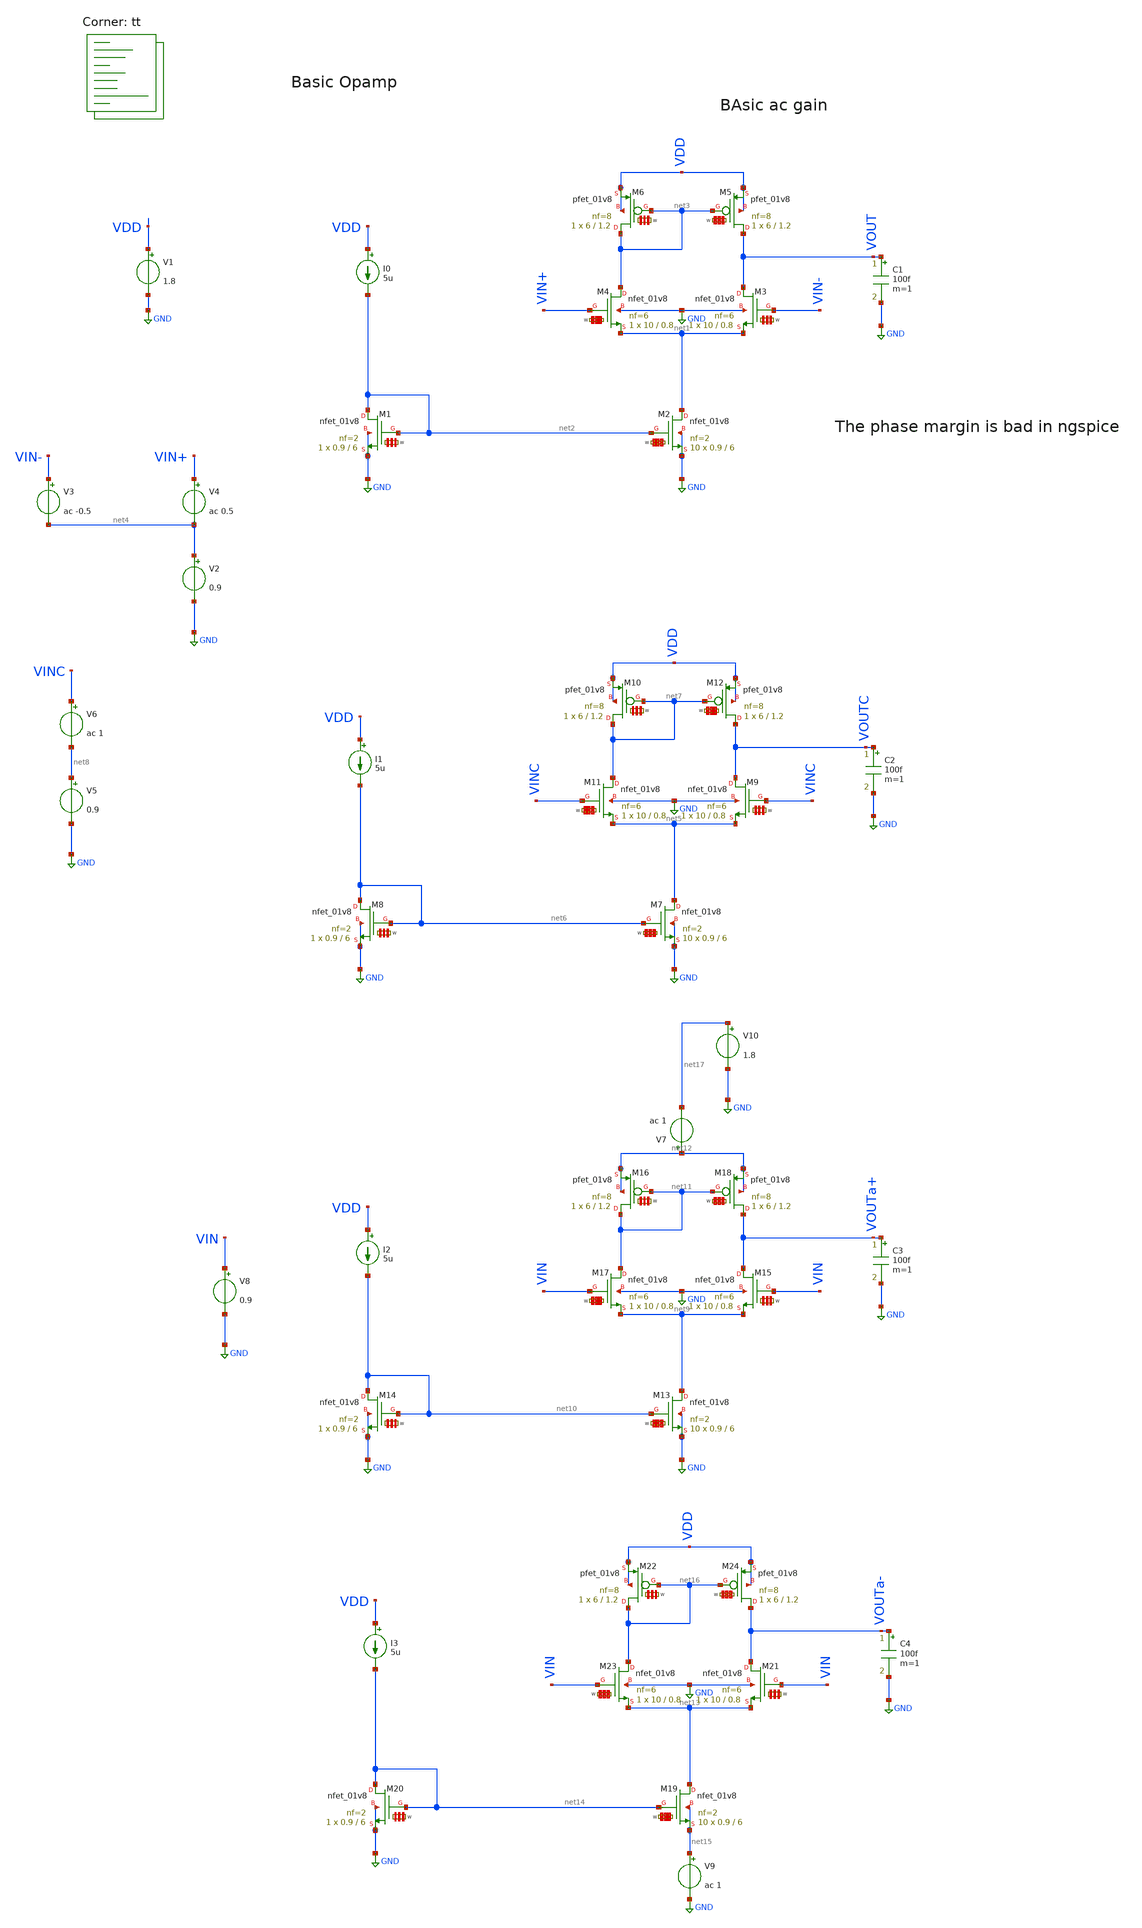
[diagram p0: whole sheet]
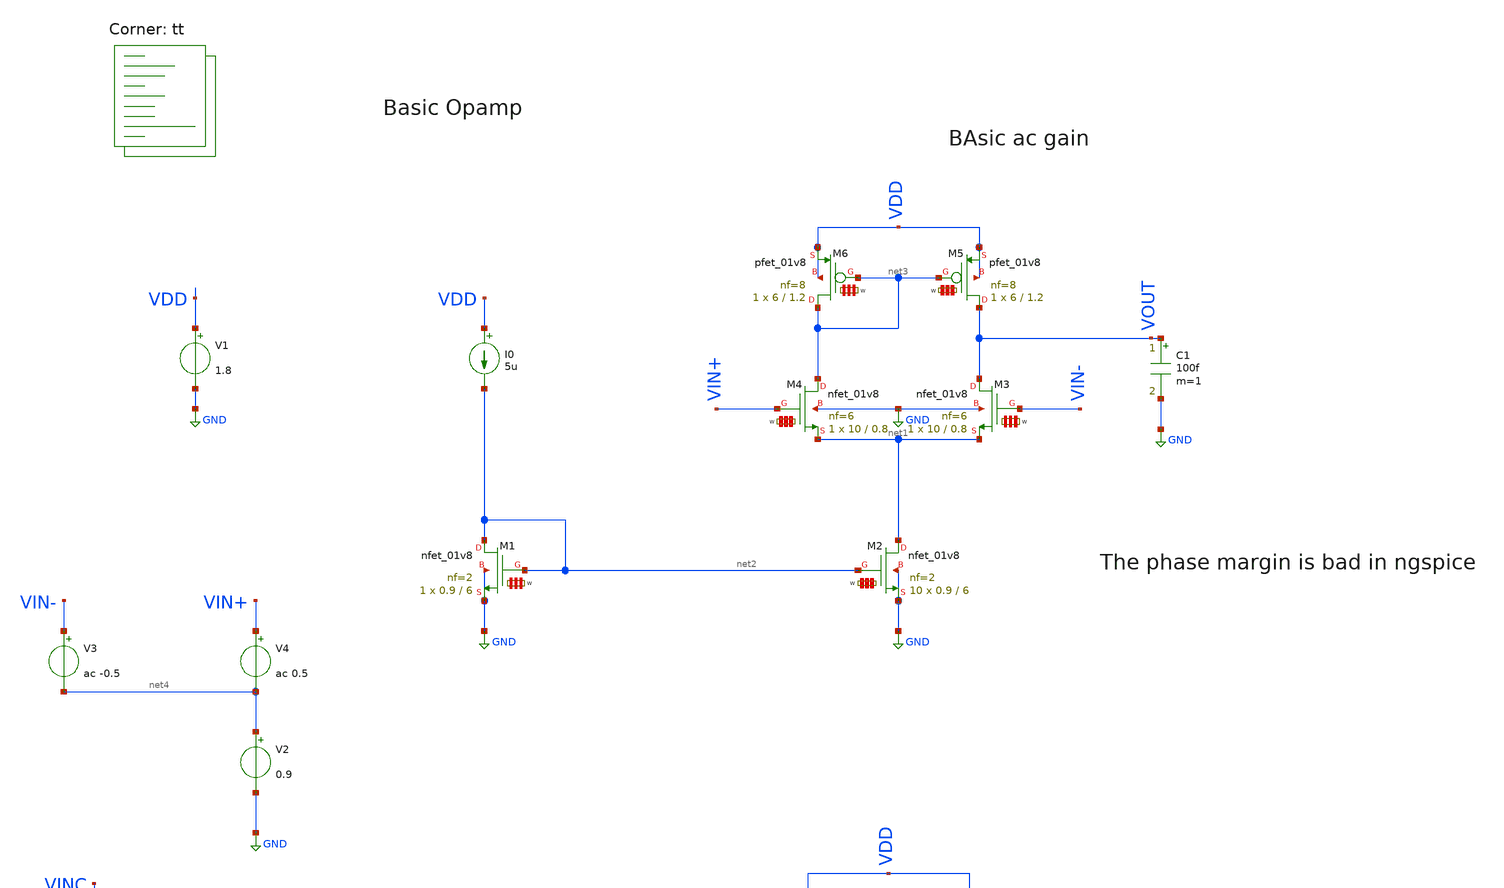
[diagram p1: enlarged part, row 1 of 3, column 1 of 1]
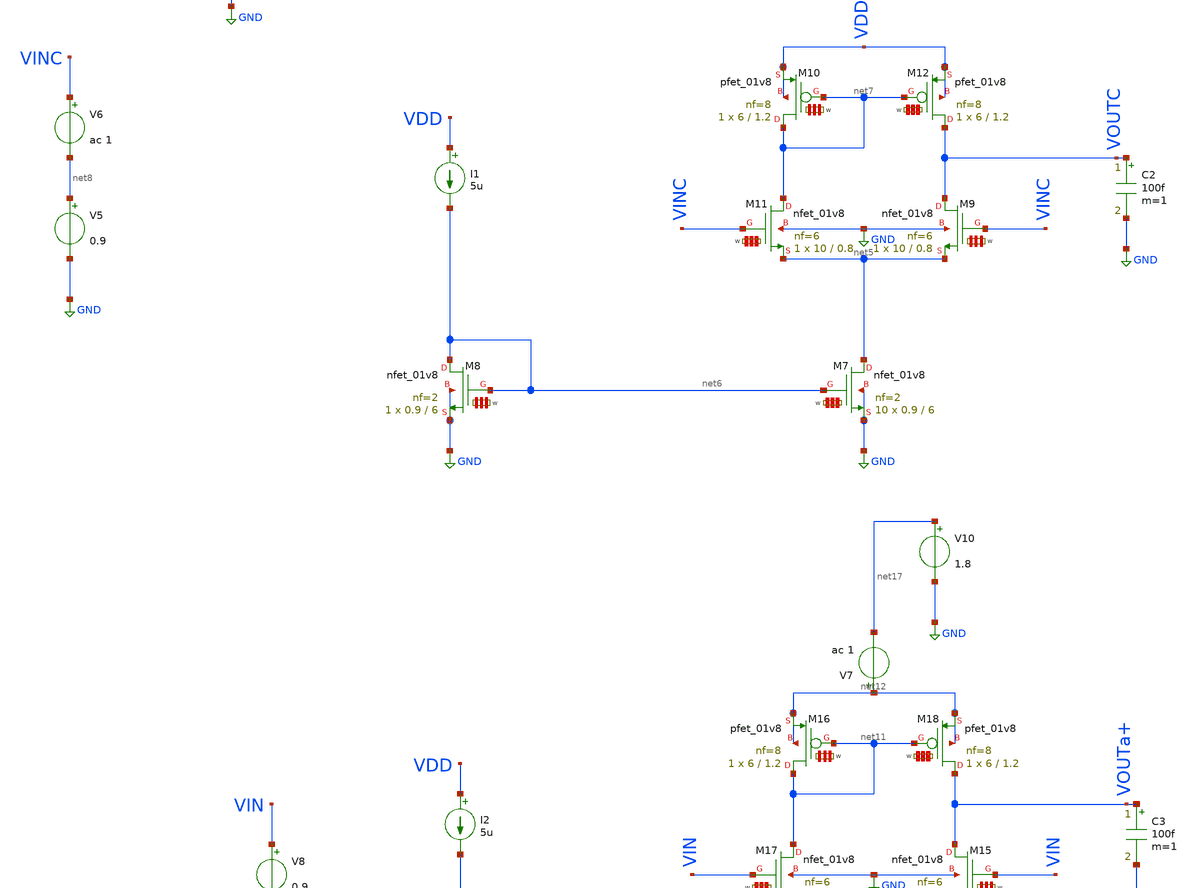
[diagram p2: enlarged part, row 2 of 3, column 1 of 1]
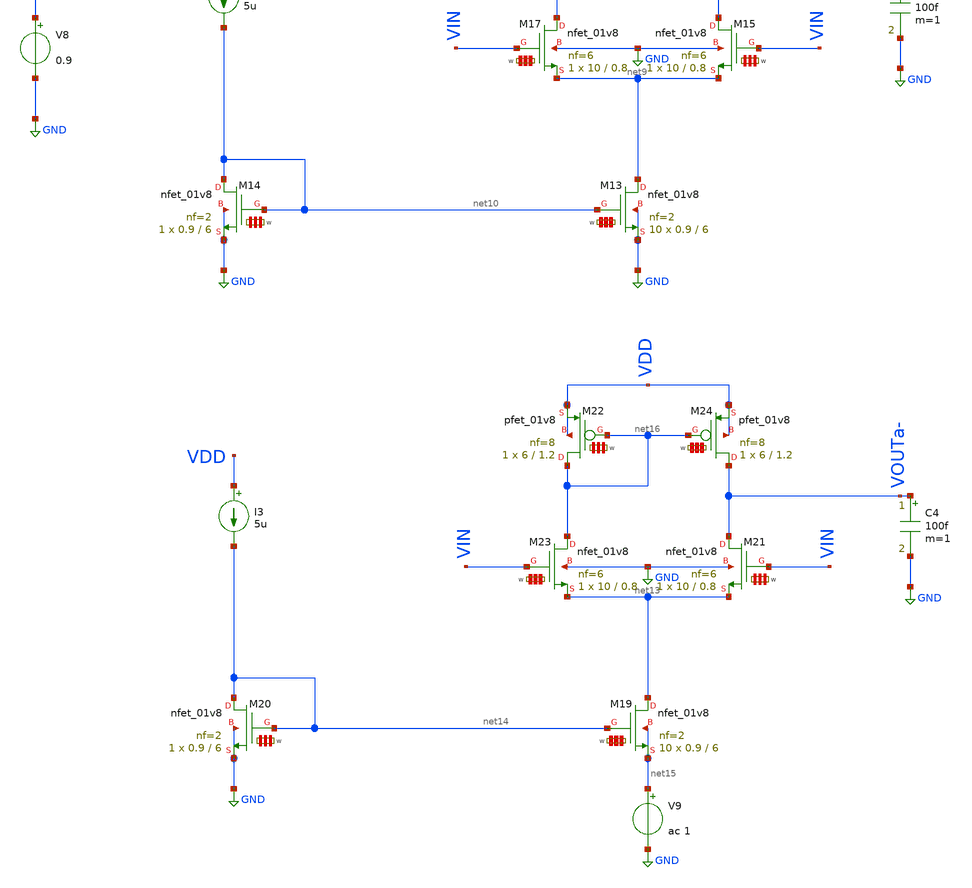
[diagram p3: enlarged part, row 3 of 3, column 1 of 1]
** sch_path: my_ip/sky130A/PMOS_2_stage_1_8_opamp_V1/NMOS.sch
**.subckt NMOS
V1 VDD GND 1.8
I0 VDD net2 5u
XM2 net1 net2 GND GND sky130_fd_pr__nfet_01v8 L=6 W='0.9 * 2 ' nf=2 ad='int((2 + 1)/2) * 0.9 / 2 * 0.29'
+ as='int((2 + 2)/2) * 0.9 / 2 * 0.29' pd='2*int((2 + 1)/2) * (0.9 / 2 + 0.29)' ps='2*int((2 + 2)/2) * (0.9 / 2 + 0.29)'
+ nrd='0.29 / 0.9 ' nrs='0.29 / 0.9 ' sa=0 sb=0 sd=0 mult=10 m=10
XM1 net2 net2 GND GND sky130_fd_pr__nfet_01v8 L=6 W='0.9 * 2 ' nf=2 ad='int((2 + 1)/2) * 0.9 / 2 * 0.29'
+ as='int((2 + 2)/2) * 0.9 / 2 * 0.29' pd='2*int((2 + 1)/2) * (0.9 / 2 + 0.29)' ps='2*int((2 + 2)/2) * (0.9 / 2 + 0.29)'
+ nrd='0.29 / 0.9 ' nrs='0.29 / 0.9 ' sa=0 sb=0 sd=0 mult=1 m=1
XM3 VOUT VIN- net1 GND sky130_fd_pr__nfet_01v8 L=0.8 W='10 * 6 ' nf=6 ad='int((6 + 1)/2) * 10 / 6 * 0.29'
+ as='int((6 + 2)/2) * 10 / 6 * 0.29' pd='2*int((6 + 1)/2) * (10 / 6 + 0.29)' ps='2*int((6 + 2)/2) * (10 / 6 + 0.29)'
+ nrd='0.29 / 10 ' nrs='0.29 / 10 ' sa=0 sb=0 sd=0 mult=1 m=1
XM6 net3 net3 VDD VDD sky130_fd_pr__pfet_01v8 L=1.2 W='6 * 8 ' nf=8 ad= as='int((8 + 2)/2) * 6 * 0.29'
+ pd='2*int((8 + 1)/2) * (6 + 0.29)' ps='2*int((8 + 2)/2) * (6 + 0.29)' nrd='0.29 / 6 / 8 ' nrs='0.29 / 6 / 8 '
+ sa=0 sb=0 sd=0 mult=1 m=1
C1 VOUT GND 100f m=1
XM4 net3 VIN+ net1 GND sky130_fd_pr__nfet_01v8 L=0.8 W='10 * 6 ' nf=6 ad='int((6 + 1)/2) * 10 / 6 * 0.29'
+ as='int((6 + 2)/2) * 10 / 6 * 0.29' pd='2*int((6 + 1)/2) * (10 / 6 + 0.29)' ps='2*int((6 + 2)/2) * (10 / 6 + 0.29)'
+ nrd='0.29 / 10 ' nrs='0.29 / 10 ' sa=0 sb=0 sd=0 mult=1 m=1
XM5 VOUT net3 VDD VDD sky130_fd_pr__pfet_01v8 L=1.2 W='6 * 8 ' nf=8 ad= as='int((8 + 2)/2) * 6 * 0.29'
+ pd='2*int((8 + 1)/2) * (6 + 0.29)' ps='2*int((8 + 2)/2) * (6 + 0.29)' nrd='0.29 / 6 / 8 ' nrs='0.29 / 6 / 8 '
+ sa=0 sb=0 sd=0 mult=1 m=1
V2 net4 GND 0.9
V4 VIN+ net4 ac 0.5
V3 VIN- net4 ac -0.5
I1 VDD net6 5u
XM7 net5 net6 GND GND sky130_fd_pr__nfet_01v8 L=6 W='0.9 * 2 ' nf=2 ad='int((2 + 1)/2) * 0.9 / 2 * 0.29'
+ as='int((2 + 2)/2) * 0.9 / 2 * 0.29' pd='2*int((2 + 1)/2) * (0.9 / 2 + 0.29)' ps='2*int((2 + 2)/2) * (0.9 / 2 + 0.29)'
+ nrd='0.29 / 0.9 ' nrs='0.29 / 0.9 ' sa=0 sb=0 sd=0 mult=10 m=10
XM8 net6 net6 GND GND sky130_fd_pr__nfet_01v8 L=6 W='0.9 * 2 ' nf=2 ad='int((2 + 1)/2) * 0.9 / 2 * 0.29'
+ as='int((2 + 2)/2) * 0.9 / 2 * 0.29' pd='2*int((2 + 1)/2) * (0.9 / 2 + 0.29)' ps='2*int((2 + 2)/2) * (0.9 / 2 + 0.29)'
+ nrd='0.29 / 0.9 ' nrs='0.29 / 0.9 ' sa=0 sb=0 sd=0 mult=1 m=1
XM9 VOUTC VINC net5 GND sky130_fd_pr__nfet_01v8 L=0.8 W='10 * 6 ' nf=6 ad='int((6 + 1)/2) * 10 / 6 * 0.29'
+ as='int((6 + 2)/2) * 10 / 6 * 0.29' pd='2*int((6 + 1)/2) * (10 / 6 + 0.29)' ps='2*int((6 + 2)/2) * (10 / 6 + 0.29)'
+ nrd='0.29 / 10 ' nrs='0.29 / 10 ' sa=0 sb=0 sd=0 mult=1 m=1
XM10 net7 net7 VDD VDD sky130_fd_pr__pfet_01v8 L=1.2 W='6 * 8 ' nf=8 ad= as='int((8 + 2)/2) * 6 * 0.29'
+ pd='2*int((8 + 1)/2) * (6 + 0.29)' ps='2*int((8 + 2)/2) * (6 + 0.29)' nrd='0.29 / 6 / 8 ' nrs='0.29 / 6 / 8 '
+ sa=0 sb=0 sd=0 mult=1 m=1
C2 VOUTC GND 100f m=1
XM11 net7 VINC net5 GND sky130_fd_pr__nfet_01v8 L=0.8 W='10 * 6 ' nf=6 ad='int((6 + 1)/2) * 10 / 6 * 0.29'
+ as='int((6 + 2)/2) * 10 / 6 * 0.29' pd='2*int((6 + 1)/2) * (10 / 6 + 0.29)' ps='2*int((6 + 2)/2) * (10 / 6 + 0.29)'
+ nrd='0.29 / 10 ' nrs='0.29 / 10 ' sa=0 sb=0 sd=0 mult=1 m=1
XM12 VOUTC net7 VDD VDD sky130_fd_pr__pfet_01v8 L=1.2 W='6 * 8 ' nf=8 ad= as='int((8 + 2)/2) * 6 * 0.29'
+ pd='2*int((8 + 1)/2) * (6 + 0.29)' ps='2*int((8 + 2)/2) * (6 + 0.29)' nrd='0.29 / 6 / 8 ' nrs='0.29 / 6 / 8 '
+ sa=0 sb=0 sd=0 mult=1 m=1
V5 net8 GND 0.9
V6 VINC net8 ac 1
I2 VDD net10 5u
XM13 net9 net10 GND GND sky130_fd_pr__nfet_01v8 L=6 W='0.9 * 2 ' nf=2 ad='int((2 + 1)/2) * 0.9 / 2 * 0.29'
+ as='int((2 + 2)/2) * 0.9 / 2 * 0.29' pd='2*int((2 + 1)/2) * (0.9 / 2 + 0.29)' ps='2*int((2 + 2)/2) * (0.9 / 2 + 0.29)'
+ nrd='0.29 / 0.9 ' nrs='0.29 / 0.9 ' sa=0 sb=0 sd=0 mult=10 m=10
XM14 net10 net10 GND GND sky130_fd_pr__nfet_01v8 L=6 W='0.9 * 2 ' nf=2 ad='int((2 + 1)/2) * 0.9 / 2 * 0.29'
+ as='int((2 + 2)/2) * 0.9 / 2 * 0.29' pd='2*int((2 + 1)/2) * (0.9 / 2 + 0.29)' ps='2*int((2 + 2)/2) * (0.9 / 2 + 0.29)'
+ nrd='0.29 / 0.9 ' nrs='0.29 / 0.9 ' sa=0 sb=0 sd=0 mult=1 m=1
XM15 VOUTa+ VIN net9 GND sky130_fd_pr__nfet_01v8 L=0.8 W='10 * 6 ' nf=6 ad='int((6 + 1)/2) * 10 / 6 * 0.29'
+ as='int((6 + 2)/2) * 10 / 6 * 0.29' pd='2*int((6 + 1)/2) * (10 / 6 + 0.29)' ps='2*int((6 + 2)/2) * (10 / 6 + 0.29)'
+ nrd='0.29 / 10 ' nrs='0.29 / 10 ' sa=0 sb=0 sd=0 mult=1 m=1
XM16 net11 net11 net12 net12 sky130_fd_pr__pfet_01v8 L=1.2 W='6 * 8 ' nf=8 ad= as='int((8 + 2)/2) * 6 * 0.29'
+ pd='2*int((8 + 1)/2) * (6 + 0.29)' ps='2*int((8 + 2)/2) * (6 + 0.29)' nrd='0.29 / 6 / 8 ' nrs='0.29 / 6 / 8 '
+ sa=0 sb=0 sd=0 mult=1 m=1
C3 VOUTa+ GND 100f m=1
XM17 net11 VIN net9 GND sky130_fd_pr__nfet_01v8 L=0.8 W='10 * 6 ' nf=6 ad='int((6 + 1)/2) * 10 / 6 * 0.29'
+ as='int((6 + 2)/2) * 10 / 6 * 0.29' pd='2*int((6 + 1)/2) * (10 / 6 + 0.29)' ps='2*int((6 + 2)/2) * (10 / 6 + 0.29)'
+ nrd='0.29 / 10 ' nrs='0.29 / 10 ' sa=0 sb=0 sd=0 mult=1 m=1
XM18 VOUTa+ net11 net12 net12 sky130_fd_pr__pfet_01v8 L=1.2 W='6 * 8 ' nf=8 ad= as='int((8 + 2)/2) * 6 * 0.29'
+ pd='2*int((8 + 1)/2) * (6 + 0.29)' ps='2*int((8 + 2)/2) * (6 + 0.29)' nrd='0.29 / 6 / 8 ' nrs='0.29 / 6 / 8 '
+ sa=0 sb=0 sd=0 mult=1 m=1
V7 net12 net17 ac 1
V8 VIN GND 0.9
I3 VDD net14 5u
XM19 net13 net14 net15 net15 sky130_fd_pr__nfet_01v8 L=6 W='0.9 * 2 ' nf=2 ad='int((2 + 1)/2) * 0.9 / 2 * 0.29'
+ as='int((2 + 2)/2) * 0.9 / 2 * 0.29' pd='2*int((2 + 1)/2) * (0.9 / 2 + 0.29)' ps='2*int((2 + 2)/2) * (0.9 / 2 + 0.29)'
+ nrd='0.29 / 0.9 ' nrs='0.29 / 0.9 ' sa=0 sb=0 sd=0 mult=10 m=10
XM20 net14 net14 GND GND sky130_fd_pr__nfet_01v8 L=6 W='0.9 * 2 ' nf=2 ad='int((2 + 1)/2) * 0.9 / 2 * 0.29'
+ as='int((2 + 2)/2) * 0.9 / 2 * 0.29' pd='2*int((2 + 1)/2) * (0.9 / 2 + 0.29)' ps='2*int((2 + 2)/2) * (0.9 / 2 + 0.29)'
+ nrd='0.29 / 0.9 ' nrs='0.29 / 0.9 ' sa=0 sb=0 sd=0 mult=1 m=1
XM21 VOUTa- VIN net13 GND sky130_fd_pr__nfet_01v8 L=0.8 W='10 * 6 ' nf=6 ad='int((6 + 1)/2) * 10 / 6 * 0.29'
+ as='int((6 + 2)/2) * 10 / 6 * 0.29' pd='2*int((6 + 1)/2) * (10 / 6 + 0.29)' ps='2*int((6 + 2)/2) * (10 / 6 + 0.29)'
+ nrd='0.29 / 10 ' nrs='0.29 / 10 ' sa=0 sb=0 sd=0 mult=1 m=1
XM22 net16 net16 VDD VDD sky130_fd_pr__pfet_01v8 L=1.2 W='6 * 8 ' nf=8 ad= as='int((8 + 2)/2) * 6 * 0.29'
+ pd='2*int((8 + 1)/2) * (6 + 0.29)' ps='2*int((8 + 2)/2) * (6 + 0.29)' nrd='0.29 / 6 / 8 ' nrs='0.29 / 6 / 8 '
+ sa=0 sb=0 sd=0 mult=1 m=1
C4 VOUTa- GND 100f m=1
XM23 net16 VIN net13 GND sky130_fd_pr__nfet_01v8 L=0.8 W='10 * 6 ' nf=6 ad='int((6 + 1)/2) * 10 / 6 * 0.29'
+ as='int((6 + 2)/2) * 10 / 6 * 0.29' pd='2*int((6 + 1)/2) * (10 / 6 + 0.29)' ps='2*int((6 + 2)/2) * (10 / 6 + 0.29)'
+ nrd='0.29 / 10 ' nrs='0.29 / 10 ' sa=0 sb=0 sd=0 mult=1 m=1
XM24 VOUTa- net16 VDD VDD sky130_fd_pr__pfet_01v8 L=1.2 W='6 * 8 ' nf=8 ad= as='int((8 + 2)/2) * 6 * 0.29'
+ pd='2*int((8 + 1)/2) * (6 + 0.29)' ps='2*int((8 + 2)/2) * (6 + 0.29)' nrd='0.29 / 6 / 8 ' nrs='0.29 / 6 / 8 '
+ sa=0 sb=0 sd=0 mult=1 m=1
V9 net15 GND ac 1
V10 net17 GND 1.8
**** begin user architecture code
.lib $::SKYWATER_MODELS/sky130.lib.spice tt

**************************************************************
**************************************************************
**************************************************************
**************************************************************
**************************************************************
*LIBs*********************************************************
**************************************************************
**************************************************************
**************************************************************
**************************************************************
**************************************************************
*.lib $::SKYWATER_MODELS/sky130.lib.spice tt
* chose the corners in the corner file
* tt_mm for mismatch
* ss ff sf fs standart corners
* ll hh lh hl capacitor and resistors corners
* mc for total process variation including corners
**************************************************************
**************************************************************
**************************************************************
**************************************************************
**************************************************************
*Corners/montecarlo options***********************************
**************************************************************
**************************************************************
**************************************************************
**************************************************************
**************************************************************
.TEMP 27
**************************************************************
**************************************************************
**************************************************************
**************************************************************
*SIMULATION and Plots*****************************************
**************************************************************
**************************************************************
**************************************************************
**************************************************************
.control
save all
ac dec 20 1 50G
plot db(v(VOUT))
plot (180*ph(v(VOUT))/pi)
plot (db(v(VOUT))-db(v(VOUTC)))
plot (db(v(VOUT))-db(v(VOUTa+)))
plot (db(v(VOUT))-db(v(VOUTa-)))
.endc

**** end user architecture code
**.ends
.GLOBAL GND
.end
